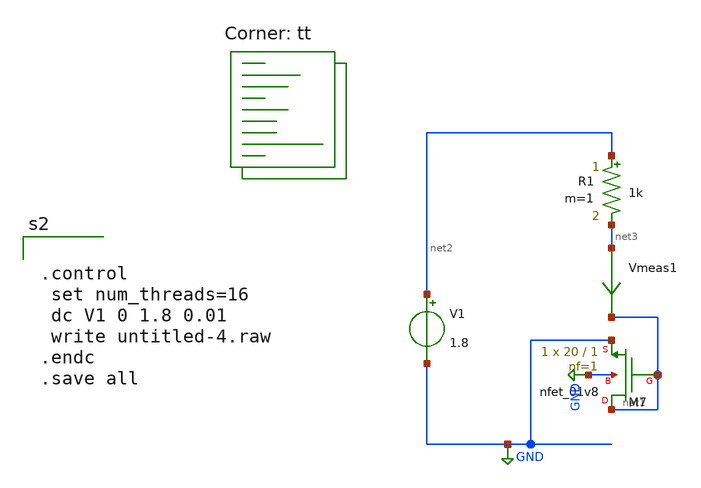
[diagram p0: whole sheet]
** sch_path: tests/untitled-4.sch
**.subckt untitled-4
XM7 net1 net1 GND GND sky130_fd_pr__nfet_01v8 L=1 W=20 nf=1 ad='int((1 + 1)/2) * 20 / 1 * 0.29' as='int((1 + 2)/2) * 20 / 1 * 0.29'
+ pd='2*int((1 + 1)/2) * (20 / 1 + 0.29)' ps='2*int((1 + 2)/2) * (20 / 1 + 0.29)' nrd='0.29 / 20 ' nrs='0.29 / 20 '
+ sa=0 sb=0 sd=0 mult=1 m=1
R1 net2 net3 1k m=1
V1 net2 GND 1.8
Vmeas1 net3 net1 0
.save i(vmeas1)
**** begin user architecture code


.control
 set num_threads=16
 dc V1 0 1.8 0.01
 write untitled-4.raw
.endc
.save all


.lib $::SKYWATER_MODELS/sky130.lib.spice tt

.subckt rram_cell BE TE gap_i=0.1
N1 BE TE rram_model
.model rram_model rram gap_initial={gap_i}
.ends rram_cell

.control
pre_osdi /foss/designs/spike_130/designs/prubs/rram.osdi
.endc

**** end user architecture code
**.ends
.GLOBAL GND
.end
